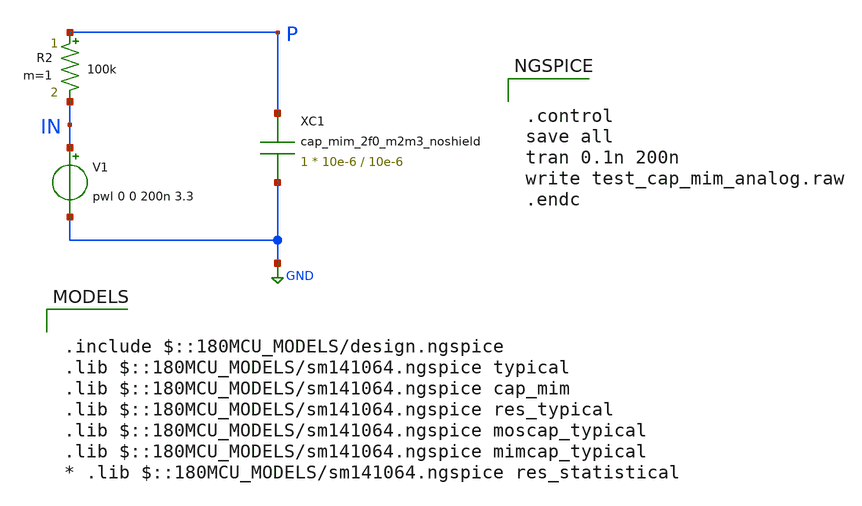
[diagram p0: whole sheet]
** sch_path: gf180mcuD/xschem_libs/gf180mcu_tests/test_cap_mim_analog/schematic/test_cap_mim_analog.sch
* Copyright 2022 GlobalFoundries PDK Authors
* Licensed under the Apache License, Version 2.0 (the "License");
* you may not use this file except in compliance with the License.
* You may obtain a copy of the License at
* https://www.apache.org/licenses/LICENSE-2.0
* Unless required by applicable law or agreed to in writing, software
* distributed under the License is distributed on an "AS IS" BASIS,
* WITHOUT WARRANTIES OR CONDITIONS OF ANY KIND, either express or implied.
* See the License for the specific language governing permissions and
* limitations under the License.
**.subckt test_cap_mim_analog
XC1 P GND cap_mim_2f0_m2m3_noshield c_width=10e-6 c_length=10e-6 m=1
V1 IN GND pwl 0 0 200n 3.3
R2 P IN 100k m=1
**** begin user architecture code

.include $::180MCU_MODELS/design.ngspice
.lib $::180MCU_MODELS/sm141064.ngspice typical
.lib $::180MCU_MODELS/sm141064.ngspice cap_mim
.lib $::180MCU_MODELS/sm141064.ngspice res_typical
.lib $::180MCU_MODELS/sm141064.ngspice moscap_typical
.lib $::180MCU_MODELS/sm141064.ngspice mimcap_typical
* .lib $::180MCU_MODELS/sm141064.ngspice res_statistical



.control
save all
tran 0.1n 200n
write test_cap_mim_analog.raw
.endc


**** end user architecture code
**.ends
.GLOBAL GND
.end
